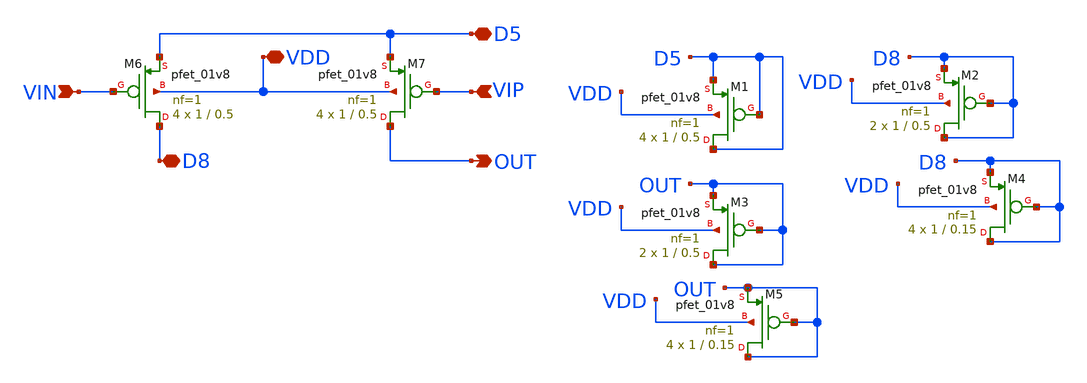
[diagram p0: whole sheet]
** sch_path: opamp/mag/pmos_out2.sch
**.subckt pmos_out2 VIP VIN D8 D5 VDD OUT
*.ipin VIP
*.ipin VIN
*.iopin D8
*.iopin D5
*.iopin VDD
*.opin OUT
XM6 D8 VIN D5 VDD sky130_fd_pr__pfet_01v8 L=0.5 W=1 nf=1 ad='int((nf+1)/2) * W/nf * 0.29' as='int((nf+2)/2) * W/nf * 0.29'
+ pd='2*int((nf+1)/2) * (W/nf + 0.29)' ps='2*int((nf+2)/2) * (W/nf + 0.29)' nrd='0.29 / W' nrs='0.29 / W'
+ sa=0 sb=0 sd=0 mult=4 m=4
XM7 OUT VIP D5 VDD sky130_fd_pr__pfet_01v8 L=0.5 W=1 nf=1 ad='int((nf+1)/2) * W/nf * 0.29' as='int((nf+2)/2) * W/nf * 0.29'
+ pd='2*int((nf+1)/2) * (W/nf + 0.29)' ps='2*int((nf+2)/2) * (W/nf + 0.29)' nrd='0.29 / W' nrs='0.29 / W'
+ sa=0 sb=0 sd=0 mult=4 m=4
XM1 D5 D5 D5 VDD sky130_fd_pr__pfet_01v8 L=0.5 W=1 nf=1 ad='int((nf+1)/2) * W/nf * 0.29' as='int((nf+2)/2) * W/nf * 0.29'
+ pd='2*int((nf+1)/2) * (W/nf + 0.29)' ps='2*int((nf+2)/2) * (W/nf + 0.29)' nrd='0.29 / W' nrs='0.29 / W'
+ sa=0 sb=0 sd=0 mult=4 m=4
XM2 D8 D8 D8 VDD sky130_fd_pr__pfet_01v8 L=0.5 W=1 nf=1 ad='int((nf+1)/2) * W/nf * 0.29' as='int((nf+2)/2) * W/nf * 0.29'
+ pd='2*int((nf+1)/2) * (W/nf + 0.29)' ps='2*int((nf+2)/2) * (W/nf + 0.29)' nrd='0.29 / W' nrs='0.29 / W'
+ sa=0 sb=0 sd=0 mult=2 m=2
XM3 OUT OUT OUT VDD sky130_fd_pr__pfet_01v8 L=0.5 W=1 nf=1 ad='int((nf+1)/2) * W/nf * 0.29' as='int((nf+2)/2) * W/nf * 0.29'
+ pd='2*int((nf+1)/2) * (W/nf + 0.29)' ps='2*int((nf+2)/2) * (W/nf + 0.29)' nrd='0.29 / W' nrs='0.29 / W'
+ sa=0 sb=0 sd=0 mult=2 m=2
XM4 D8 D8 D8 VDD sky130_fd_pr__pfet_01v8 L=0.15 W=1 nf=1 ad='int((nf+1)/2) * W/nf * 0.29' as='int((nf+2)/2) * W/nf * 0.29'
+ pd='2*int((nf+1)/2) * (W/nf + 0.29)' ps='2*int((nf+2)/2) * (W/nf + 0.29)' nrd='0.29 / W' nrs='0.29 / W'
+ sa=0 sb=0 sd=0 mult=4 m=4
XM5 OUT OUT OUT VDD sky130_fd_pr__pfet_01v8 L=0.15 W=1 nf=1 ad='int((nf+1)/2) * W/nf * 0.29' as='int((nf+2)/2) * W/nf * 0.29'
+ pd='2*int((nf+1)/2) * (W/nf + 0.29)' ps='2*int((nf+2)/2) * (W/nf + 0.29)' nrd='0.29 / W' nrs='0.29 / W'
+ sa=0 sb=0 sd=0 mult=4 m=4
**.ends
.end
